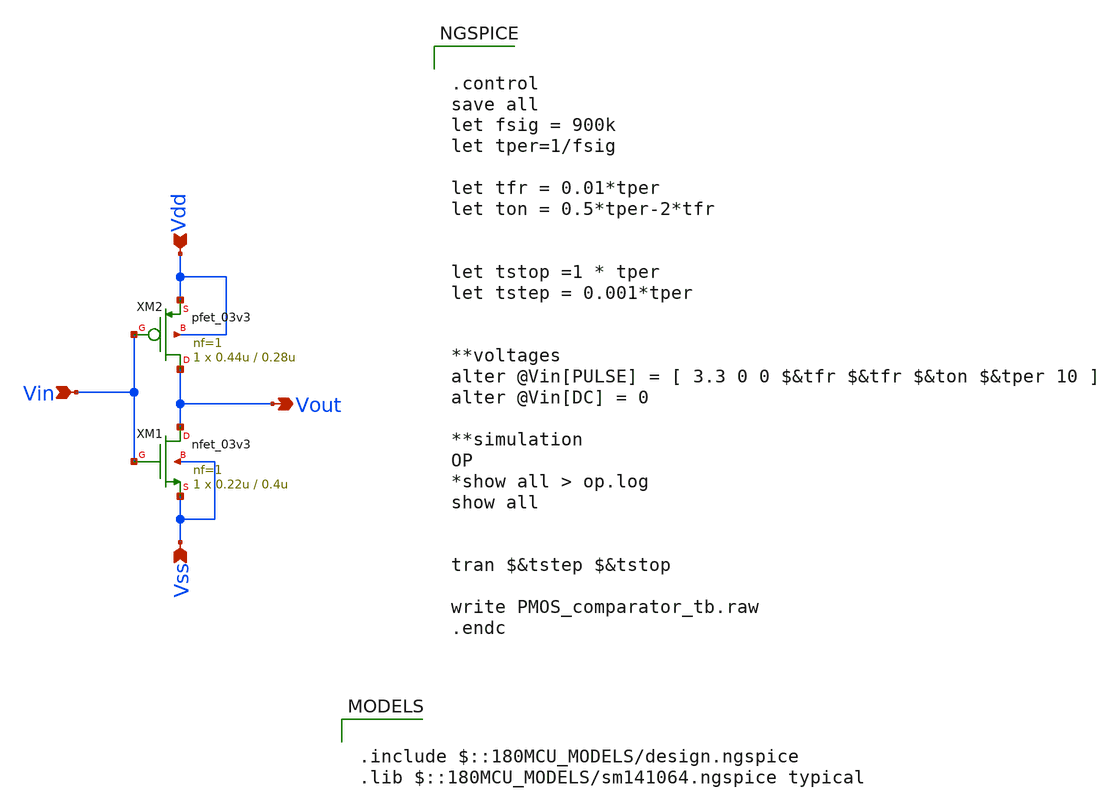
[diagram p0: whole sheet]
** sch_path: designs/libs/core_analog/Gates/Inverter.sch
**.subckt Inverter Vin Vdd Vss Vout
*.ipin Vin
*.ipin Vdd
*.ipin Vss
*.opin Vout
XM1 Vout Vin Vss Vss nfet_03v3 L=0.4u W=0.22u nf=1 ad='int((nf+1)/2) * W/nf * 0.18u' as='int((nf+2)/2) * W/nf * 0.18u'
+ pd='2*int((nf+1)/2) * (W/nf + 0.18u)' ps='2*int((nf+2)/2) * (W/nf + 0.18u)' nrd='0.18u / W' nrs='0.18u / W'
+ sa=0 sb=0 sd=0 m=1
XM2 Vout Vin Vdd Vdd pfet_03v3 L=0.28u W=0.44u nf=1 ad='int((nf+1)/2) * W/nf * 0.18u' as='int((nf+2)/2) * W/nf * 0.18u'
+ pd='2*int((nf+1)/2) * (W/nf + 0.18u)' ps='2*int((nf+2)/2) * (W/nf + 0.18u)' nrd='0.18u / W' nrs='0.18u / W'
+ sa=0 sb=0 sd=0 m=1
**** begin user architecture code


.control
save all
let fsig = 900k
let tper=1/fsig

let tfr = 0.01*tper
let ton = 0.5*tper-2*tfr


let tstop =1 * tper
let tstep = 0.001*tper


**voltages
alter @Vin[PULSE] = [ 3.3 0 0 $&tfr $&tfr $&ton $&tper 10 ]
alter @Vin[DC] = 0

**simulation
OP
*show all > op.log
show all


tran $&tstep $&tstop

write PMOS_comparator_tb.raw
.endc



.include $::180MCU_MODELS/design.ngspice
.lib $::180MCU_MODELS/sm141064.ngspice typical

**** end user architecture code
**.ends
.end
